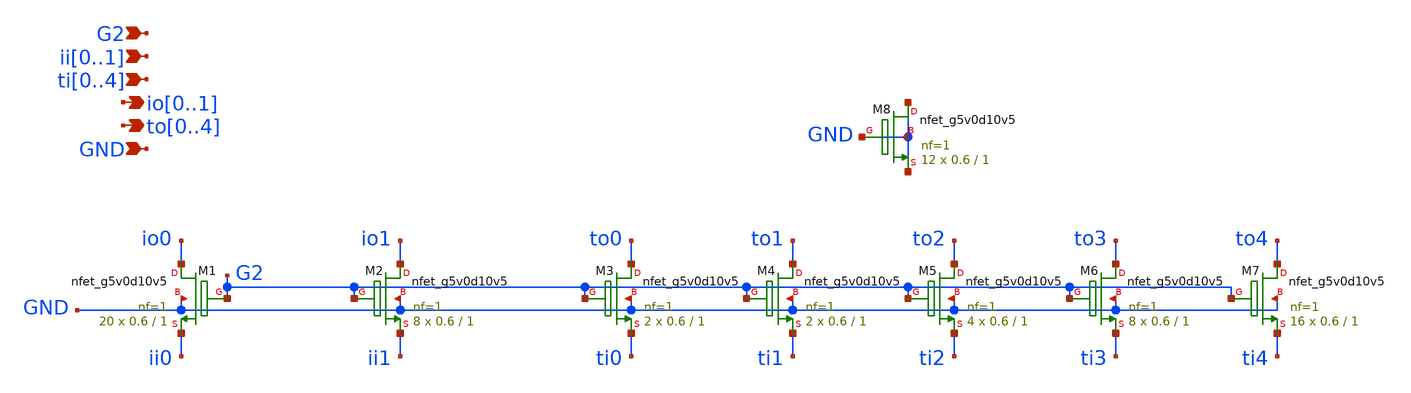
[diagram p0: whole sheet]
** sch_path: xschem/cm_ncell2.sch
**.subckt cm_ncell2 G2 io0,io1 GND to0,to1,to2,to3,to4 ii0,ii1 ti0,ti1,ti2,ti3,ti4
*.ipin G2
*.opin io0,io1
*.ipin GND
*.opin to0,to1,to2,to3,to4
*.ipin ii0,ii1
*.ipin ti0,ti1,ti2,ti3,ti4
XM1 io0 G2 ii0 GND sky130_fd_pr__nfet_g5v0d10v5 L=1 W=0.6 nf=1 ad='int((nf+1)/2) * W/nf * 0.29' as='int((nf+2)/2) * W/nf * 0.29'
+ pd='2*int((nf+1)/2) * (W/nf + 0.29)' ps='2*int((nf+2)/2) * (W/nf + 0.29)' nrd='0.29 / W' nrs='0.29 / W'
+ sa=0 sb=0 sd=0 mult=20 m=20
XM2 io1 G2 ii1 GND sky130_fd_pr__nfet_g5v0d10v5 L=1 W=0.6 nf=1 ad='int((nf+1)/2) * W/nf * 0.29' as='int((nf+2)/2) * W/nf * 0.29'
+ pd='2*int((nf+1)/2) * (W/nf + 0.29)' ps='2*int((nf+2)/2) * (W/nf + 0.29)' nrd='0.29 / W' nrs='0.29 / W'
+ sa=0 sb=0 sd=0 mult=8 m=8
XM3 to0 G2 ti0 GND sky130_fd_pr__nfet_g5v0d10v5 L=1 W=0.6 nf=1 ad='int((nf+1)/2) * W/nf * 0.29' as='int((nf+2)/2) * W/nf * 0.29'
+ pd='2*int((nf+1)/2) * (W/nf + 0.29)' ps='2*int((nf+2)/2) * (W/nf + 0.29)' nrd='0.29 / W' nrs='0.29 / W'
+ sa=0 sb=0 sd=0 mult=2 m=2
XM5 to2 G2 ti2 GND sky130_fd_pr__nfet_g5v0d10v5 L=1 W=0.6 nf=1 ad='int((nf+1)/2) * W/nf * 0.29' as='int((nf+2)/2) * W/nf * 0.29'
+ pd='2*int((nf+1)/2) * (W/nf + 0.29)' ps='2*int((nf+2)/2) * (W/nf + 0.29)' nrd='0.29 / W' nrs='0.29 / W'
+ sa=0 sb=0 sd=0 mult=4 m=4
XM6 to3 G2 ti3 GND sky130_fd_pr__nfet_g5v0d10v5 L=1 W=0.6 nf=1 ad='int((nf+1)/2) * W/nf * 0.29' as='int((nf+2)/2) * W/nf * 0.29'
+ pd='2*int((nf+1)/2) * (W/nf + 0.29)' ps='2*int((nf+2)/2) * (W/nf + 0.29)' nrd='0.29 / W' nrs='0.29 / W'
+ sa=0 sb=0 sd=0 mult=8 m=8
XM7 to4 G2 ti4 GND sky130_fd_pr__nfet_g5v0d10v5 L=1 W=0.6 nf=1 ad='int((nf+1)/2) * W/nf * 0.29' as='int((nf+2)/2) * W/nf * 0.29'
+ pd='2*int((nf+1)/2) * (W/nf + 0.29)' ps='2*int((nf+2)/2) * (W/nf + 0.29)' nrd='0.29 / W' nrs='0.29 / W'
+ sa=0 sb=0 sd=0 mult=16 m=16
XM4 to1 G2 ti1 GND sky130_fd_pr__nfet_g5v0d10v5 L=1 W=0.6 nf=1 ad='int((nf+1)/2) * W/nf * 0.29' as='int((nf+2)/2) * W/nf * 0.29'
+ pd='2*int((nf+1)/2) * (W/nf + 0.29)' ps='2*int((nf+2)/2) * (W/nf + 0.29)' nrd='0.29 / W' nrs='0.29 / W'
+ sa=0 sb=0 sd=0 mult=2 m=2
XM8 GND GND GND GND sky130_fd_pr__nfet_g5v0d10v5 L=1 W=0.6 nf=1 ad='int((nf+1)/2) * W/nf * 0.29' as='int((nf+2)/2) * W/nf * 0.29'
+ pd='2*int((nf+1)/2) * (W/nf + 0.29)' ps='2*int((nf+2)/2) * (W/nf + 0.29)' nrd='0.29 / W' nrs='0.29 / W'
+ sa=0 sb=0 sd=0 mult=12 m=12
**.ends
.end
